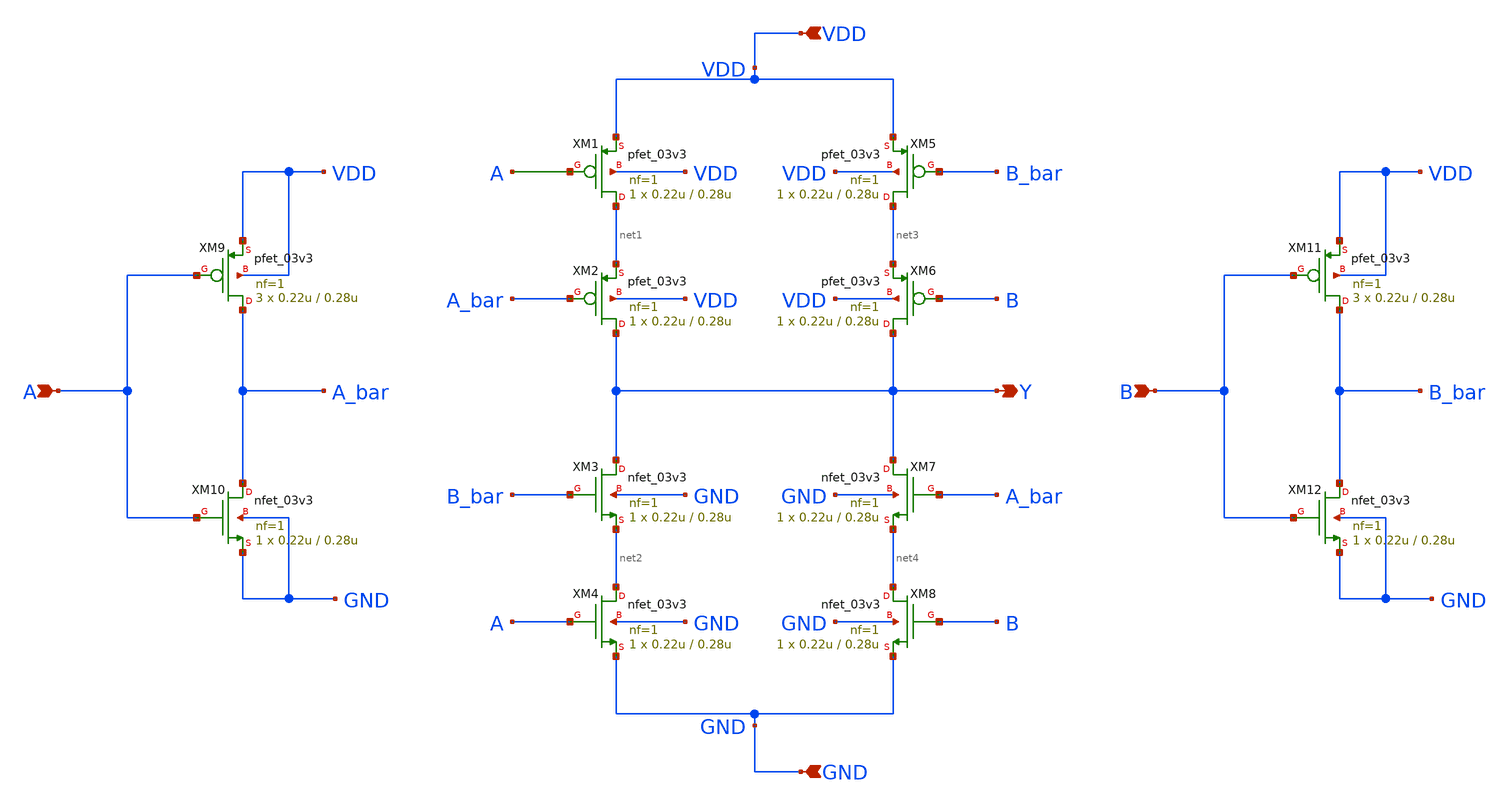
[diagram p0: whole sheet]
** sch_path: PFD/XNOR.sch
**.subckt XNOR Y VDD GND A B
*.opin Y
*.ipin VDD
*.ipin GND
*.ipin A
*.ipin B
XM1 net1 net5 VDD VDD pfet_03v3 L=0.28u W=0.22u nf=1 ad='int((nf+1)/2) * W/nf * 0.18u' as='int((nf+2)/2) * W/nf * 0.18u'
+ pd='2*int((nf+1)/2) * (W/nf + 0.18u)' ps='2*int((nf+2)/2) * (W/nf + 0.18u)' nrd='0.18u / W' nrs='0.18u / W'
+ sa=0 sb=0 sd=0 m=1
XM2 Y A_bar net1 VDD pfet_03v3 L=0.28u W=0.22u nf=1 ad='int((nf+1)/2) * W/nf * 0.18u' as='int((nf+2)/2) * W/nf * 0.18u'
+ pd='2*int((nf+1)/2) * (W/nf + 0.18u)' ps='2*int((nf+2)/2) * (W/nf + 0.18u)' nrd='0.18u / W' nrs='0.18u / W'
+ sa=0 sb=0 sd=0 m=1
XM3 Y B_bar net2 GND nfet_03v3 L=0.28u W=0.22u nf=1 ad='int((nf+1)/2) * W/nf * 0.18u' as='int((nf+2)/2) * W/nf * 0.18u'
+ pd='2*int((nf+1)/2) * (W/nf + 0.18u)' ps='2*int((nf+2)/2) * (W/nf + 0.18u)' nrd='0.18u / W' nrs='0.18u / W'
+ sa=0 sb=0 sd=0 m=1
XM4 net2 A GND GND nfet_03v3 L=0.28u W=0.22u nf=1 ad='int((nf+1)/2) * W/nf * 0.18u' as='int((nf+2)/2) * W/nf * 0.18u'
+ pd='2*int((nf+1)/2) * (W/nf + 0.18u)' ps='2*int((nf+2)/2) * (W/nf + 0.18u)' nrd='0.18u / W' nrs='0.18u / W'
+ sa=0 sb=0 sd=0 m=1
XM5 net3 B_bar VDD VDD pfet_03v3 L=0.28u W=0.22u nf=1 ad='int((nf+1)/2) * W/nf * 0.18u' as='int((nf+2)/2) * W/nf * 0.18u'
+ pd='2*int((nf+1)/2) * (W/nf + 0.18u)' ps='2*int((nf+2)/2) * (W/nf + 0.18u)' nrd='0.18u / W' nrs='0.18u / W'
+ sa=0 sb=0 sd=0 m=1
XM6 Y B net3 VDD pfet_03v3 L=0.28u W=0.22u nf=1 ad='int((nf+1)/2) * W/nf * 0.18u' as='int((nf+2)/2) * W/nf * 0.18u'
+ pd='2*int((nf+1)/2) * (W/nf + 0.18u)' ps='2*int((nf+2)/2) * (W/nf + 0.18u)' nrd='0.18u / W' nrs='0.18u / W'
+ sa=0 sb=0 sd=0 m=1
XM7 Y A_bar net4 GND nfet_03v3 L=0.28u W=0.22u nf=1 ad='int((nf+1)/2) * W/nf * 0.18u' as='int((nf+2)/2) * W/nf * 0.18u'
+ pd='2*int((nf+1)/2) * (W/nf + 0.18u)' ps='2*int((nf+2)/2) * (W/nf + 0.18u)' nrd='0.18u / W' nrs='0.18u / W'
+ sa=0 sb=0 sd=0 m=1
XM8 net4 B GND GND nfet_03v3 L=0.28u W=0.22u nf=1 ad='int((nf+1)/2) * W/nf * 0.18u' as='int((nf+2)/2) * W/nf * 0.18u'
+ pd='2*int((nf+1)/2) * (W/nf + 0.18u)' ps='2*int((nf+2)/2) * (W/nf + 0.18u)' nrd='0.18u / W' nrs='0.18u / W'
+ sa=0 sb=0 sd=0 m=1
XM9 A_bar A VDD VDD pfet_03v3 L=0.28u W=0.22u nf=1 ad='int((nf+1)/2) * W/nf * 0.18u' as='int((nf+2)/2) * W/nf * 0.18u'
+ pd='2*int((nf+1)/2) * (W/nf + 0.18u)' ps='2*int((nf+2)/2) * (W/nf + 0.18u)' nrd='0.18u / W' nrs='0.18u / W'
+ sa=0 sb=0 sd=0 m=3
XM10 A_bar A GND GND nfet_03v3 L=0.28u W=0.22u nf=1 ad='int((nf+1)/2) * W/nf * 0.18u' as='int((nf+2)/2) * W/nf * 0.18u'
+ pd='2*int((nf+1)/2) * (W/nf + 0.18u)' ps='2*int((nf+2)/2) * (W/nf + 0.18u)' nrd='0.18u / W' nrs='0.18u / W'
+ sa=0 sb=0 sd=0 m=1
XM11 B_bar B VDD VDD pfet_03v3 L=0.28u W=0.22u nf=1 ad='int((nf+1)/2) * W/nf * 0.18u' as='int((nf+2)/2) * W/nf * 0.18u'
+ pd='2*int((nf+1)/2) * (W/nf + 0.18u)' ps='2*int((nf+2)/2) * (W/nf + 0.18u)' nrd='0.18u / W' nrs='0.18u / W'
+ sa=0 sb=0 sd=0 m=3
XM12 B_bar B GND GND nfet_03v3 L=0.28u W=0.22u nf=1 ad='int((nf+1)/2) * W/nf * 0.18u' as='int((nf+2)/2) * W/nf * 0.18u'
+ pd='2*int((nf+1)/2) * (W/nf + 0.18u)' ps='2*int((nf+2)/2) * (W/nf + 0.18u)' nrd='0.18u / W' nrs='0.18u / W'
+ sa=0 sb=0 sd=0 m=1
**.ends
.end
